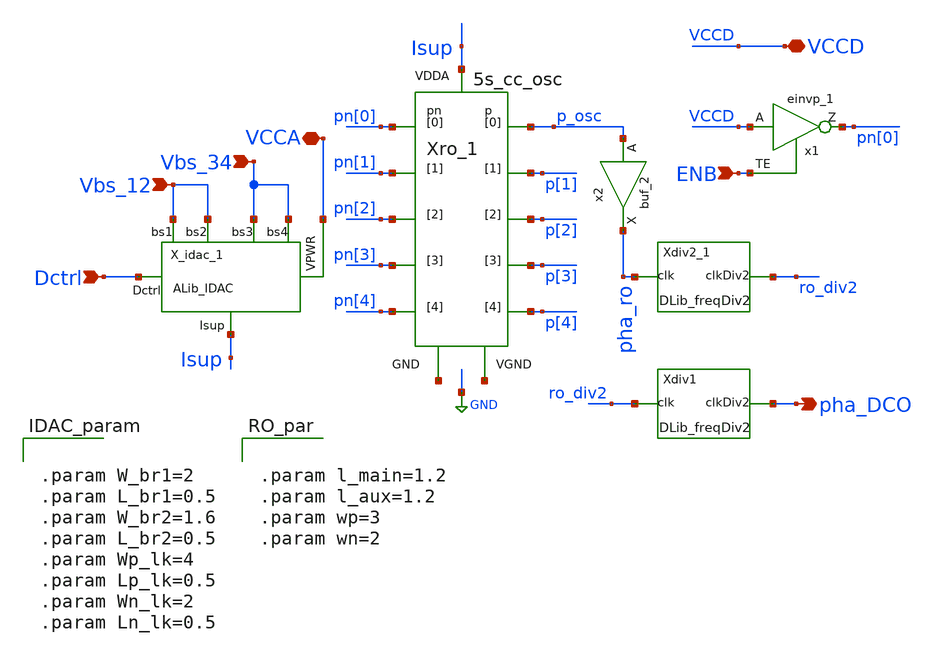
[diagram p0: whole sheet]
** sch_path: xschem/lib/ALib_DCO.sch
**.subckt ALib_DCO Dctrl Vbs_12 Vbs_34 VCCA pha_DCO VCCD ENB
*.ipin Dctrl
*.ipin Vbs_12
*.ipin Vbs_34
*.iopin VCCA
*.opin pha_DCO
*.iopin VCCD
*.ipin ENB
x1 VCCD ENB VGND VNB VPB VPWR pn[0] sky130_fd_sc_hd__einvp_1
X_idac_1 Dctrl Vbs_12 Vbs_12 Vbs_34 Vbs_34 VCCA Isup ALib_IDAC W_br1="W_br1" L_br1="L_br1"
+ W_br2="W_br2" L_br2="L_br2" Wp_lk="Wp_lk" Lp_lk="Lp_lk" Wn_lk="Wn_lk" Ln_lk="Wn_lk"
x2 p_osc GND GND VCCD VCCD pha_ro sky130_fd_sc_hd__buf_2
Xdiv2_1 pha_ro GND GND VCCD VCCD ro_div2 DLib_freqDiv2
Xro_1 net1 Isup p_osc p[1] p[2] p[3] p[4] pn[0] pn[1] pn[2] pn[3] pn[4] net2 5s_cc_osc
Xdiv1 ro_div2 GND GND VCCD VCCD pha_DCO DLib_freqDiv2
**** begin user architecture code


.param W_br1=2
.param L_br1=0.5
.param W_br2=1.6
.param L_br2=0.5
.param Wp_lk=4
.param Lp_lk=0.5
.param Wn_lk=2
.param Ln_lk=0.5

**** end user architecture code
**.ends
.GLOBAL GND
**** begin user architecture code


.param l_main=1.2
.param l_aux=1.2
.param wp=3
.param wn=2

**** end user architecture code
.end
